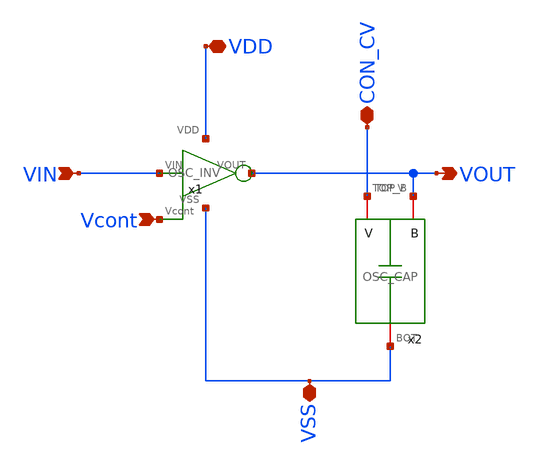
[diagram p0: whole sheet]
** sch_path: ABC123_SDC/design_data/xschem/OSC_STAGE/OSC_STAGE.sch
**.subckt OSC_STAGE VIN VDD VOUT CON_CV VSS Vcont
*.ipin VIN
*.iopin VDD
*.opin VOUT
*.iopin CON_CV
*.iopin VSS
*.ipin Vcont
x1 VDD VIN VOUT VSS Vcont OSC_INV
x2 VOUT CON_CV VSS OSC_CAP
**.ends
.end
